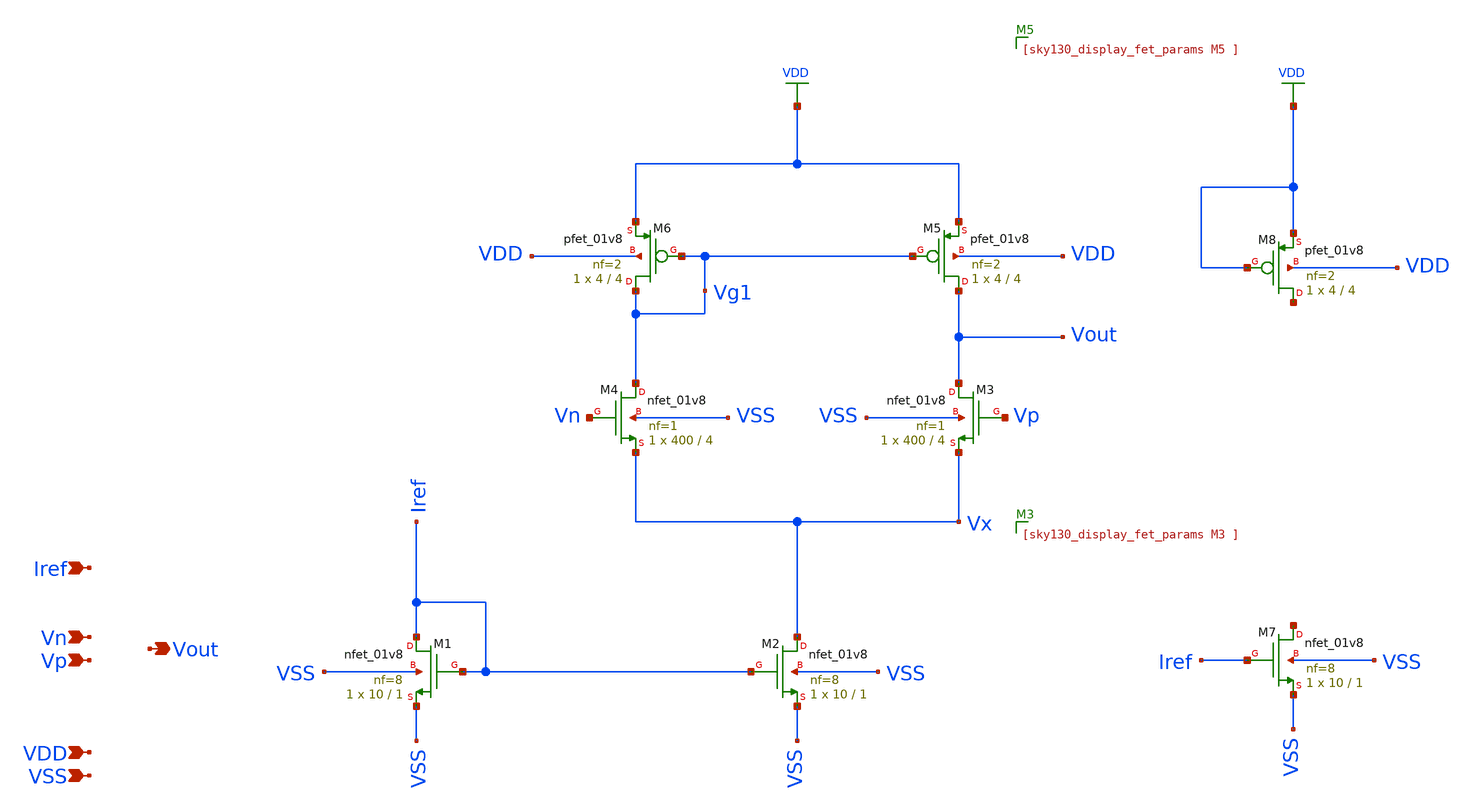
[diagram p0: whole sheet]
** sch_path: xschem/opamp.sch
**.subckt opamp VSS Vp Vout Vn VDD Iref
*.ipin VSS
*.ipin Vp
*.opin Vout
*.ipin Vn
*.ipin VDD
*.ipin Iref
XM1 Iref Iref VSS VSS sky130_fd_pr__nfet_01v8 L=1 W=10 nf=8 ad='int((8 + 1)/2) * 10 / 8 * 0.29' as='int((8 + 2)/2) * 10 / 8 * 0.29'
+ pd='2*int((8 + 1)/2) * (10 / 8 + 0.29)' ps='2*int((8 + 2)/2) * (10 / 8 + 0.29)' nrd='0.29 / 10 ' nrs='0.29 / 10 '
+ sa=0 sb=0 sd=0 mult=1 m=1
XM2 Vx Iref VSS VSS sky130_fd_pr__nfet_01v8 L=1 W=10 nf=8 ad='int((8 + 1)/2) * 10 / 8 * 0.29' as='int((8 + 2)/2) * 10 / 8 * 0.29'
+ pd='2*int((8 + 1)/2) * (10 / 8 + 0.29)' ps='2*int((8 + 2)/2) * (10 / 8 + 0.29)' nrd='0.29 / 10 ' nrs='0.29 / 10 '
+ sa=0 sb=0 sd=0 mult=1 m=1
XM3 Vout Vp Vx VSS sky130_fd_pr__nfet_01v8 L=4 W=400 nf=1 ad='int((1 + 1)/2) * 400 / 1 * 0.29' as='int((1 + 2)/2) * 400 / 1 * 0.29'
+ pd='2*int((1 + 1)/2) * (400 / 1 + 0.29)' ps='2*int((1 + 2)/2) * (400 / 1 + 0.29)' nrd='0.29 / 400 ' nrs='0.29 / 400 '
+ sa=0 sb=0 sd=0 mult=1 m=1
XM4 Vg1 Vn Vx VSS sky130_fd_pr__nfet_01v8 L=4 W=400 nf=1 ad='int((1 + 1)/2) * 400 / 1 * 0.29' as='int((1 + 2)/2) * 400 / 1 * 0.29'
+ pd='2*int((1 + 1)/2) * (400 / 1 + 0.29)' ps='2*int((1 + 2)/2) * (400 / 1 + 0.29)' nrd='0.29 / 400 ' nrs='0.29 / 400 '
+ sa=0 sb=0 sd=0 mult=1 m=1
XM5 Vout Vg1 VDD VDD sky130_fd_pr__pfet_01v8 L=4 W=4 nf=2 ad='int((2 + 1)/2) * 4 / 2 * 0.29' as='int((2 + 2)/2) * 4 / 2 * 0.29'
+ pd='2*int((2 + 1)/2) * (4 / 2 + 0.29)' ps='2*int((2 + 2)/2) * (4 / 2 + 0.29)' nrd='0.29 / 4 ' nrs='0.29 / 4 '
+ sa=0 sb=0 sd=0 mult=1 m=1
XM6 Vg1 Vg1 VDD VDD sky130_fd_pr__pfet_01v8 L=4 W=4 nf=2 ad='int((2 + 1)/2) * 4 / 2 * 0.29' as='int((2 + 2)/2) * 4 / 2 * 0.29'
+ pd='2*int((2 + 1)/2) * (4 / 2 + 0.29)' ps='2*int((2 + 2)/2) * (4 / 2 + 0.29)' nrd='0.29 / 4 ' nrs='0.29 / 4 '
+ sa=0 sb=0 sd=0 mult=1 m=1
XM7 net1 Iref VSS VSS sky130_fd_pr__nfet_01v8 L=1 W=10 nf=8 ad='int((8 + 1)/2) * 10 / 8 * 0.29' as='int((8 + 2)/2) * 10 / 8 * 0.29'
+ pd='2*int((8 + 1)/2) * (10 / 8 + 0.29)' ps='2*int((8 + 2)/2) * (10 / 8 + 0.29)' nrd='0.29 / 10 ' nrs='0.29 / 10 '
+ sa=0 sb=0 sd=0 mult=1 m=1
XM8 net2 VDD VDD VDD sky130_fd_pr__pfet_01v8 L=4 W=4 nf=2 ad='int((2 + 1)/2) * 4 / 2 * 0.29' as='int((2 + 2)/2) * 4 / 2 * 0.29'
+ pd='2*int((2 + 1)/2) * (4 / 2 + 0.29)' ps='2*int((2 + 2)/2) * (4 / 2 + 0.29)' nrd='0.29 / 4 ' nrs='0.29 / 4 '
+ sa=0 sb=0 sd=0 mult=1 m=1
**.ends
.GLOBAL VDD
.end
